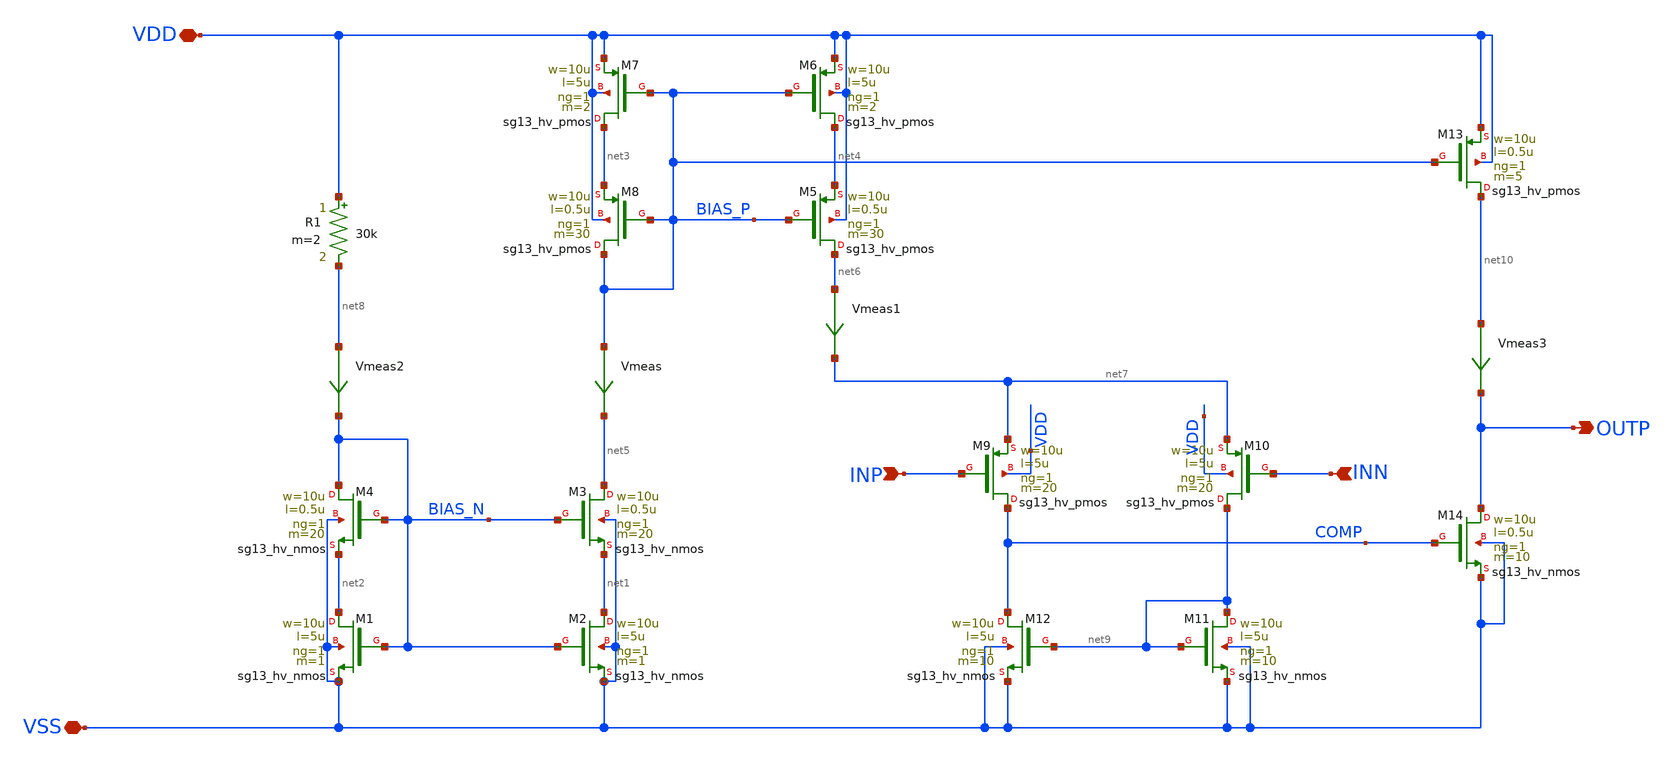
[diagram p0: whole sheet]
** sch_path: xschem/ip_amplifier.sch
**.subckt ip_amplifier VSS VDD OUTP INN INP
*.iopin VSS
*.iopin VDD
*.opin OUTP
*.ipin INN
*.ipin INP
XM1 net2 BIAS_N VSS VSS sg13_hv_nmos w=10u l=5u ng=1 m=1 mm_ok=1
R1 VDD net8 30k m=2
XM2 net1 BIAS_N VSS VSS sg13_hv_nmos w=10u l=5u ng=1 m=1 mm_ok=1
XM3 net5 BIAS_N net1 VSS sg13_hv_nmos w=10u l=0.5u ng=1 m=20 mm_ok=1
XM4 BIAS_N BIAS_N net2 VSS sg13_hv_nmos w=10u l=0.5u ng=1 m=20 mm_ok=1
Vmeas BIAS_P net5 0
Vmeas1 net6 net7 0
XM5 net6 BIAS_P net4 VDD sg13_hv_pmos w=10u l=0.5u ng=1 m=30 mm_ok=1
XM6 net4 BIAS_P VDD VDD sg13_hv_pmos w=10u l=5u ng=1 m=2 mm_ok=1
XM7 net3 BIAS_P VDD VDD sg13_hv_pmos w=10u l=5u ng=1 m=2 mm_ok=1
XM8 BIAS_P BIAS_P net3 VDD sg13_hv_pmos w=10u l=0.5u ng=1 m=30 mm_ok=1
Vmeas2 net8 BIAS_N 0
XM9 COMP INP net7 VDD sg13_hv_pmos w=10u l=5u ng=1 m=20 mm_ok=1
XM10 net9 INN net7 VDD sg13_hv_pmos w=10u l=5u ng=1 m=20 mm_ok=1
XM11 net9 net9 VSS VSS sg13_hv_nmos w=10u l=5u ng=1 m=10 mm_ok=1
XM12 COMP net9 VSS VSS sg13_hv_nmos w=10u l=5u ng=1 m=10 mm_ok=1
XM13 net10 BIAS_P VDD VDD sg13_hv_pmos w=10u l=0.5u ng=1 m=5 mm_ok=1
XM14 OUTP COMP VSS VSS sg13_hv_nmos w=10u l=0.5u ng=1 m=10 mm_ok=1
Vmeas3 net10 OUTP 0
**.ends
.end
